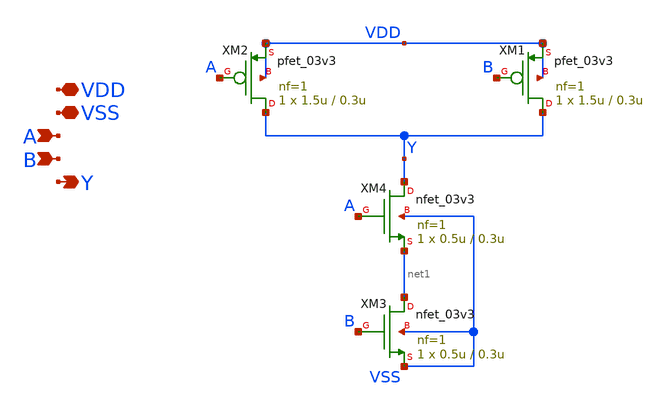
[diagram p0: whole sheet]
** sch_path: designs/libs/core_analog/switch-matrix/nand2_1.sch
**.subckt nand2_1 VDD VSS A B Y
*.iopin VDD
*.iopin VSS
*.ipin A
*.ipin B
*.opin Y
XM2 Y A VDD VDD pfet_03v3 L=0.3u W=1.5u nf=1 ad='int((nf+1)/2) * W/nf * 0.18u' as='int((nf+2)/2) * W/nf * 0.18u'
+ pd='2*int((nf+1)/2) * (W/nf + 0.18u)' ps='2*int((nf+2)/2) * (W/nf + 0.18u)' nrd='0.18u / W' nrs='0.18u / W'
+ sa=0 sb=0 sd=0 m=1
XM1 Y B VDD VDD pfet_03v3 L=0.3u W=1.5u nf=1 ad='int((nf+1)/2) * W/nf * 0.18u' as='int((nf+2)/2) * W/nf * 0.18u'
+ pd='2*int((nf+1)/2) * (W/nf + 0.18u)' ps='2*int((nf+2)/2) * (W/nf + 0.18u)' nrd='0.18u / W' nrs='0.18u / W'
+ sa=0 sb=0 sd=0 m=1
XM4 Y A net1 VSS nfet_03v3 L=0.3u W=0.5u nf=1 ad='int((nf+1)/2) * W/nf * 0.18u' as='int((nf+2)/2) * W/nf * 0.18u'
+ pd='2*int((nf+1)/2) * (W/nf + 0.18u)' ps='2*int((nf+2)/2) * (W/nf + 0.18u)' nrd='0.18u / W' nrs='0.18u / W'
+ sa=0 sb=0 sd=0 m=1
XM3 net1 B VSS VSS nfet_03v3 L=0.3u W=0.5u nf=1 ad='int((nf+1)/2) * W/nf * 0.18u' as='int((nf+2)/2) * W/nf * 0.18u'
+ pd='2*int((nf+1)/2) * (W/nf + 0.18u)' ps='2*int((nf+2)/2) * (W/nf + 0.18u)' nrd='0.18u / W' nrs='0.18u / W'
+ sa=0 sb=0 sd=0 m=1
**.ends
.end
